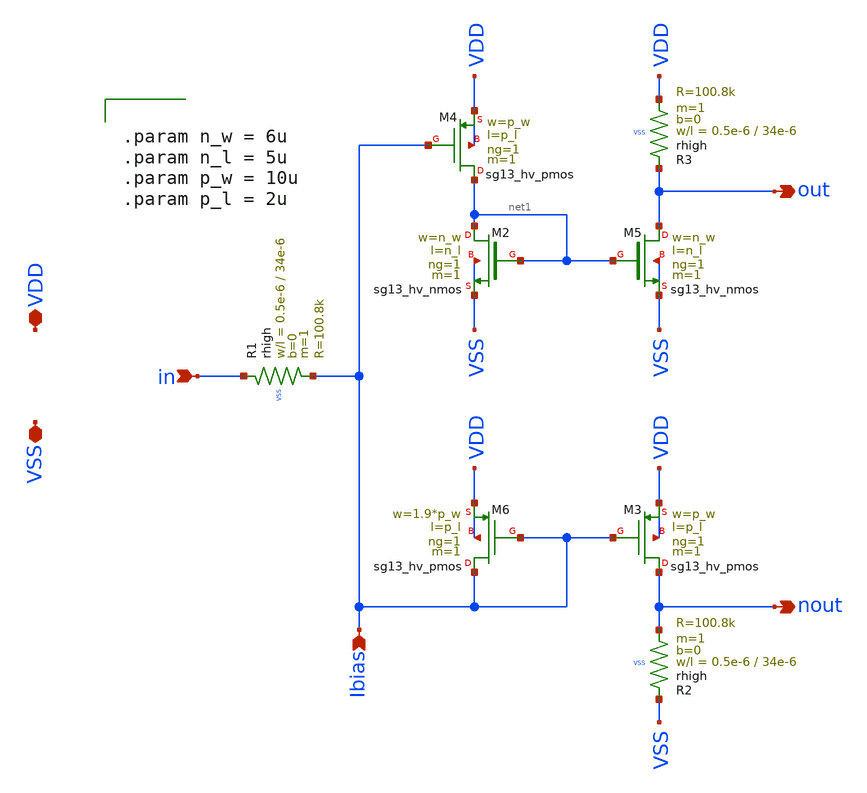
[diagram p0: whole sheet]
** sch_path: macros/heichips26_vcr/macros/switched_capacitor/schematic/xschem/voltage_mirror_pmos.sch
**.subckt voltage_mirror_pmos VDD VSS in out nout Ibias
*.iopin VDD
*.iopin VSS
*.ipin in
*.opin out
*.opin nout
*.ipin Ibias
XR1 in Ibias VSS rhigh w=0.5e-6 l=34e-6 m=1 b=0 mm_ok=1
XM4 net1 Ibias VDD VDD sg13_hv_pmos w=p_w l=p_l ng=1 m=1 mm_ok=1
XM5 out net1 VSS VSS sg13_hv_nmos w=n_w l=n_l ng=1 m=1 mm_ok=1
XR2 VSS nout VSS rhigh w=0.5e-6 l=34e-6 m=1 b=0 mm_ok=1
XR3 out VDD VSS rhigh w=0.5e-6 l=34e-6 m=1 b=0 mm_ok=1
XM2 net1 net1 VSS VSS sg13_hv_nmos w=n_w l=n_l ng=1 m=1 mm_ok=1
XM3 nout Ibias VDD VDD sg13_hv_pmos w=p_w l=p_l ng=1 m=1 mm_ok=1
XM6 Ibias Ibias VDD VDD sg13_hv_pmos w=1.9*p_w l=p_l ng=1 m=1 mm_ok=1
**** begin user architecture code


.param n_w = 6u
.param n_l = 5u
.param p_w = 10u
.param p_l = 2u


**** end user architecture code
**.ends
.end
